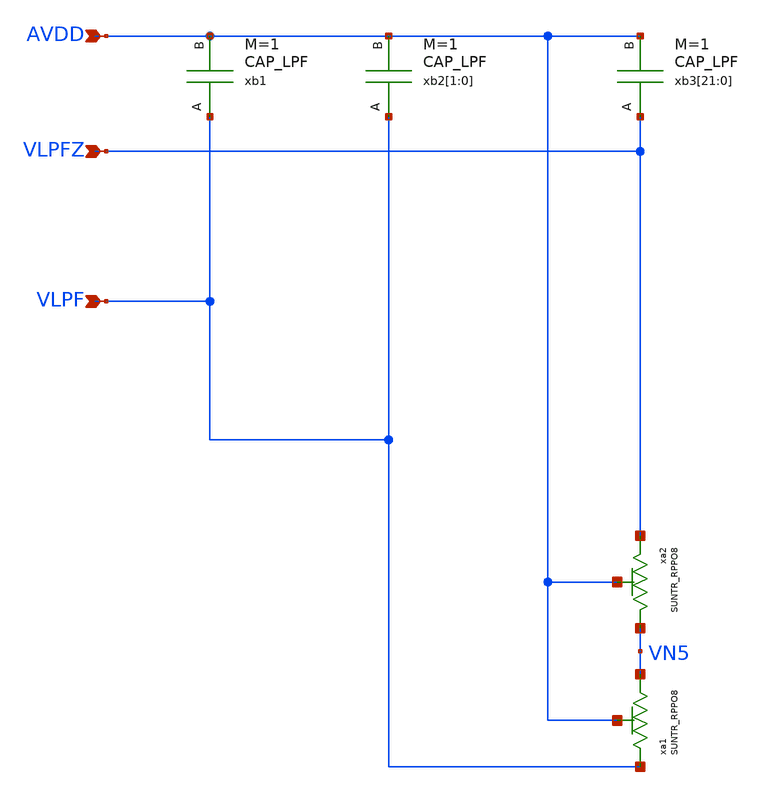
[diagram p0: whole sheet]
** sch_path: design/JNW_GR00_SKY130NM/JNWG00_LPF.sch
**.subckt JNWG00_LPF VLPF AVDD VLPFZ
*.ipin VLPF
*.ipin AVDD
*.ipin VLPFZ
xb3[21] VLPFZ AVDD CAP_LPF xoffset=0 yoffset=0 angle=0 M=1
xb3[20] VLPFZ AVDD CAP_LPF xoffset=0 yoffset=0 angle=0 M=1
xb3[19] VLPFZ AVDD CAP_LPF xoffset=0 yoffset=0 angle=0 M=1
xb3[18] VLPFZ AVDD CAP_LPF xoffset=0 yoffset=0 angle=0 M=1
xb3[17] VLPFZ AVDD CAP_LPF xoffset=0 yoffset=0 angle=0 M=1
xb3[16] VLPFZ AVDD CAP_LPF xoffset=0 yoffset=0 angle=0 M=1
xb3[15] VLPFZ AVDD CAP_LPF xoffset=0 yoffset=0 angle=0 M=1
xb3[14] VLPFZ AVDD CAP_LPF xoffset=0 yoffset=0 angle=0 M=1
xb3[13] VLPFZ AVDD CAP_LPF xoffset=0 yoffset=0 angle=0 M=1
xb3[12] VLPFZ AVDD CAP_LPF xoffset=0 yoffset=0 angle=0 M=1
xb3[11] VLPFZ AVDD CAP_LPF xoffset=0 yoffset=0 angle=0 M=1
xb3[10] VLPFZ AVDD CAP_LPF xoffset=0 yoffset=0 angle=0 M=1
xb3[9] VLPFZ AVDD CAP_LPF xoffset=0 yoffset=0 angle=0 M=1
xb3[8] VLPFZ AVDD CAP_LPF xoffset=0 yoffset=0 angle=0 M=1
xb3[7] VLPFZ AVDD CAP_LPF xoffset=0 yoffset=0 angle=0 M=1
xb3[6] VLPFZ AVDD CAP_LPF xoffset=0 yoffset=0 angle=0 M=1
xb3[5] VLPFZ AVDD CAP_LPF xoffset=0 yoffset=0 angle=0 M=1
xb3[4] VLPFZ AVDD CAP_LPF xoffset=0 yoffset=0 angle=0 M=1
xb3[3] VLPFZ AVDD CAP_LPF xoffset=0 yoffset=0 angle=0 M=1
xb3[2] VLPFZ AVDD CAP_LPF xoffset=0 yoffset=0 angle=0 M=1
xb3[1] VLPFZ AVDD CAP_LPF xoffset=0 yoffset=0 angle=0 M=1
xb3[0] VLPFZ AVDD CAP_LPF xoffset=0 yoffset=0 angle=0 M=1
xb2[1] VLPF AVDD CAP_LPF xoffset=0 yoffset=0 angle=0 M=1
xb2[0] VLPF AVDD CAP_LPF xoffset=0 yoffset=0 angle=0 M=1
xb1 VLPF AVDD CAP_LPF xoffset=0 yoffset=0 angle=0 M=1
xa2 VN5 VLPFZ AVDD SUNTR_RPPO8 xoffset=0 yoffset=2 angle=0 M=1
xa1 VN5 VLPF AVDD SUNTR_RPPO8 xoffset=0 yoffset=2 angle=0 M=1
**.ends

* expanding   symbol:  SUN_PLL_SKY130NM/CAP_LPF.sym # of pins=2
** sym_path: SUN_PLL_SKY130NM/CAP_LPF.sym
** sch_path: SUN_PLL_SKY130NM/CAP_LPF.sch
.subckt CAP_LPF A B  xoffset=0 yoffset=0 angle=0 M=1
*.iopin A
*.iopin B
R1 A NC0 sky130_fd_pr__res_generic_m1 W=0.4 L=0.4 m=1
R2 B NC1 sky130_fd_pr__res_generic_m1 W=0.4 L=0.4 m=1
.ends


* expanding   symbol:  SUN_TR_SKY130NM/SUNTR_RPPO8.sym # of pins=3
** sym_path: SUN_TR_SKY130NM/SUNTR_RPPO8.sym
** sch_path: SUN_TR_SKY130NM/SUNTR_RPPO8.sch
.subckt SUNTR_RPPO8 N P B  xoffset=0 yoffset=0 angle=0 M=1
*.iopin P
*.iopin N
*.iopin B
XXA1 N P B SUNTR_RES8 xoffset=0 yoffset=0 angle=0
.ends


* expanding   symbol:  SUN_TR_SKY130NM/SUNTR_RES8.sym # of pins=3
** sym_path: SUN_TR_SKY130NM/SUNTR_RES8.sym
** sch_path: SUN_TR_SKY130NM/SUNTR_RES8.sch
.subckt SUNTR_RES8 N P B  xoffset=0 yoffset=0 angle=0
*.iopin N
*.iopin P
*.iopin B
XR1_0 INT_0 N B sky130_fd_pr__res_high_po W=0.72 L=8.8 mult=1 m=1
XR1_1 INT_1 INT_0 B sky130_fd_pr__res_high_po W=0.72 L=8.8 mult=1 m=1
XR1_2 INT_2 INT_1 B sky130_fd_pr__res_high_po W=0.72 L=8.8 mult=1 m=1
XR1_3 INT_3 INT_2 B sky130_fd_pr__res_high_po W=0.72 L=8.8 mult=1 m=1
XR1_4 INT_4 INT_3 B sky130_fd_pr__res_high_po W=0.72 L=8.8 mult=1 m=1
XR1_5 INT_5 INT_4 B sky130_fd_pr__res_high_po W=0.72 L=8.8 mult=1 m=1
XR1_6 INT_6 INT_5 B sky130_fd_pr__res_high_po W=0.72 L=8.8 mult=1 m=1
XR1_7 P INT_6 B sky130_fd_pr__res_high_po W=0.72 L=8.8 mult=1 m=1
.ends

.end
